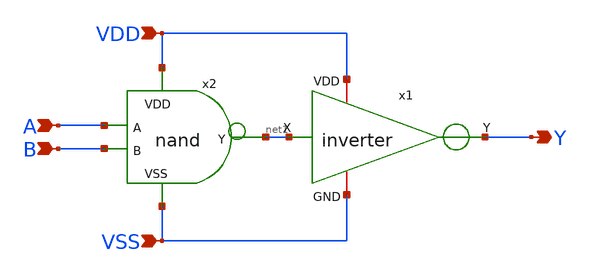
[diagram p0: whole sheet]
** sch_path: Layouts and Schematics/Spice Sim and Schem/untitled-3.sch
**.subckt untitled-3 Y VSS VDD A B
*.opin Y
*.ipin VSS
*.ipin VDD
*.ipin A
*.ipin B
x1 VDD net1 Y VSS inv
x2 VDD A net1 B VSS nand
**.ends

* expanding   symbol:  inv.sym # of pins=4
** sym_path: Layouts and Schematics/Spice Sim and Schem/inv.sym
** sch_path: Layouts and Schematics/Spice Sim and Schem/inv.sch
.subckt inv VDD X Y GND
*.ipin X
*.iopin VDD
*.iopin GND
*.opin Y
XM1 Y X GND GND sky130_fd_pr__nfet_01v8 L=0.5 W=1 nf=1 ad='int((nf+1)/2) * W/nf * 0.29' as='int((nf+2)/2) * W/nf * 0.29'
+ pd='2*int((nf+1)/2) * (W/nf + 0.29)' ps='2*int((nf+2)/2) * (W/nf + 0.29)' nrd='0.29 / W' nrs='0.29 / W'
+ sa=0 sb=0 sd=0 mult=1 m=1
XM2 Y X VDD VDD sky130_fd_pr__pfet_01v8 L=0.5 W=2 nf=1 ad='int((nf+1)/2) * W/nf * 0.29' as='int((nf+2)/2) * W/nf * 0.29'
+ pd='2*int((nf+1)/2) * (W/nf + 0.29)' ps='2*int((nf+2)/2) * (W/nf + 0.29)' nrd='0.29 / W' nrs='0.29 / W'
+ sa=0 sb=0 sd=0 mult=1 m=1
.ends


* expanding   symbol:  nand.sym # of pins=5
** sym_path: Layouts and Schematics/Spice Sim and Schem/nand.sym
** sch_path: Layouts and Schematics/Spice Sim and Schem/nand.sch
.subckt nand VDD A Y B VSS
*.ipin A
*.ipin B
*.ipin VSS
*.opin Y
*.ipin VDD
XM1 Y B net1 VSS sky130_fd_pr__nfet_01v8 L=0.5 W=2 nf=1 ad='int((nf+1)/2) * W/nf * 0.29' as='int((nf+2)/2) * W/nf * 0.29'
+ pd='2*int((nf+1)/2) * (W/nf + 0.29)' ps='2*int((nf+2)/2) * (W/nf + 0.29)' nrd='0.29 / W' nrs='0.29 / W'
+ sa=0 sb=0 sd=0 mult=1 m=1
XM3 Y B VDD VDD sky130_fd_pr__pfet_01v8 L=0.5 W=2 nf=1 ad='int((nf+1)/2) * W/nf * 0.29' as='int((nf+2)/2) * W/nf * 0.29'
+ pd='2*int((nf+1)/2) * (W/nf + 0.29)' ps='2*int((nf+2)/2) * (W/nf + 0.29)' nrd='0.29 / W' nrs='0.29 / W'
+ sa=0 sb=0 sd=0 mult=1 m=1
XM4 Y A VDD VDD sky130_fd_pr__pfet_01v8 L=0.5 W=2 nf=1 ad='int((nf+1)/2) * W/nf * 0.29' as='int((nf+2)/2) * W/nf * 0.29'
+ pd='2*int((nf+1)/2) * (W/nf + 0.29)' ps='2*int((nf+2)/2) * (W/nf + 0.29)' nrd='0.29 / W' nrs='0.29 / W'
+ sa=0 sb=0 sd=0 mult=1 m=1
XM2 net1 A VSS VSS sky130_fd_pr__nfet_01v8 L=0.5 W=2 nf=1 ad='int((nf+1)/2) * W/nf * 0.29' as='int((nf+2)/2) * W/nf * 0.29'
+ pd='2*int((nf+1)/2) * (W/nf + 0.29)' ps='2*int((nf+2)/2) * (W/nf + 0.29)' nrd='0.29 / W' nrs='0.29 / W'
+ sa=0 sb=0 sd=0 mult=1 m=1
.ends

.end
